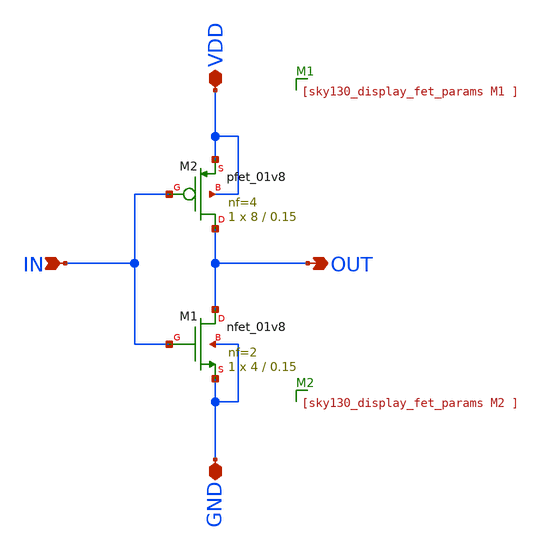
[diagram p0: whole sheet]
** sch_path: 03_magic_layout/soluzioni/lab03/xschem/inverterx4.sch
**.subckt inverterx4 IN OUT VDD GND
*.ipin IN
*.opin OUT
*.iopin VDD
*.iopin GND
XM1 OUT IN GND GND sky130_fd_pr__nfet_01v8 L=0.15 W=4 nf=2 ad='int((2 + 1)/2) * 4 / 2 * 0.29' as='int((2 + 2)/2) * 4 / 2 * 0.29'
+ pd='2*int((2 + 1)/2) * (4 / 2 + 0.29)' ps='2*int((2 + 2)/2) * (4 / 2 + 0.29)' nrd='0.29 / 4 ' nrs='0.29 / 4 '
+ sa=0 sb=0 sd=0 mult=1 m=1
XM2 OUT IN VDD VDD sky130_fd_pr__pfet_01v8 L=0.15 W=8 nf=4 ad='int((4 + 1)/2) * 8 / 4 * 0.29' as='int((4 + 2)/2) * 8 / 4 * 0.29'
+ pd='2*int((4 + 1)/2) * (8 / 4 + 0.29)' ps='2*int((4 + 2)/2) * (8 / 4 + 0.29)' nrd='0.29 / 8 ' nrs='0.29 / 8 '
+ sa=0 sb=0 sd=0 mult=1 m=1
**.ends
.end
